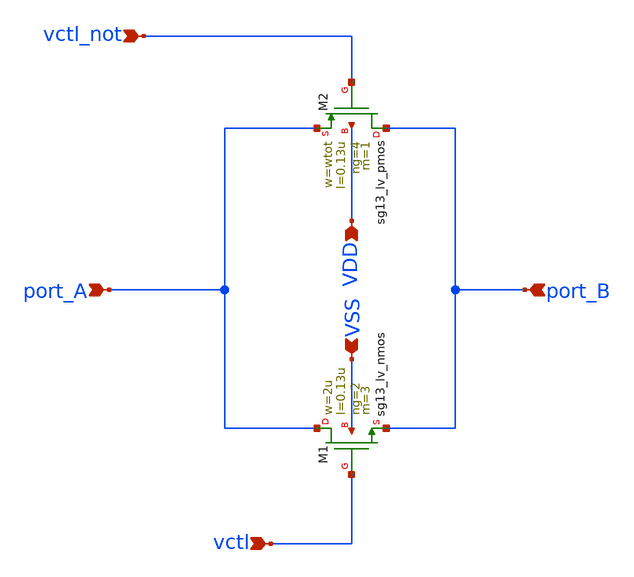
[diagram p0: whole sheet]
** sch_path: platform/packages/spicexplorer-netlist2xschem/tests/fixtures/xvport/mos_fingered.sch
**.subckt mos_fingered port_A port_B vctl VSS VDD vctl_not
*.ipin port_A
*.ipin port_B
*.ipin vctl
*.ipin VSS
*.ipin VDD
*.ipin vctl_not
XM1 port_A vctl port_B VSS sg13_lv_nmos w=2u l=0.13u ng=2 m=3 mm_ok=1
XM2 port_B vctl_not port_A VDD sg13_lv_pmos w=wtot l=0.13u ng=4 m=1 mm_ok=1
**.ends
.end
